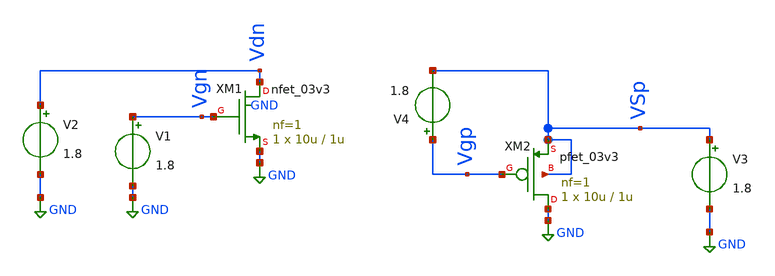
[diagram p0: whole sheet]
** sch_path: xschem/caracterizador/charac.sch
* Copyright 2022 GlobalFoundries PDK Authors
* Licensed under the Apache License, Version 2.0 (the "License");
* you may not use this file except in compliance with the License.
* You may obtain a copy of the License at
* https://www.apache.org/licenses/LICENSE-2.0
* Unless required by applicable law or agreed to in writing, software
* distributed under the License is distributed on an "AS IS" BASIS,
* WITHOUT WARRANTIES OR CONDITIONS OF ANY KIND, either express or implied.
* See the License for the specific language governing permissions and
* limitations under the License.
**.subckt charac
XM1 Vdn Vgn GND GND nfet_03v3 L=1u W=10u nf=1 ad='int((nf+1)/2) * W/nf * 0.18u' as='int((nf+2)/2) * W/nf * 0.18u'
+ pd='2*int((nf+1)/2) * (W/nf + 0.18u)' ps='2*int((nf+2)/2) * (W/nf + 0.18u)' nrd='0.18u / W' nrs='0.18u / W'
+ sa=0 sb=0 sd=0 m=1 par=1
XM2 GND Vgp VSp VSp pfet_03v3 L=1u W=10u nf=1 ad='int((nf+1)/2) * W/nf * 0.18u' as='int((nf+2)/2) * W/nf * 0.18u'
+ pd='2*int((nf+1)/2) * (W/nf + 0.18u)' ps='2*int((nf+2)/2) * (W/nf + 0.18u)' nrd='0.18u / W' nrs='0.18u / W'
+ sa=0 sb=0 sd=0 m=1 par=1
V1 Vgn GND 1.8
V2 Vdn GND 1.8
V3 VSp GND 1.8
V4 Vgp VSp 1.8
**** begin user architecture code


.include /home/ringosinye/eda/pdks/gf180mcuD/libs.tech/ngspice/design.ngspice
.lib /home/ringosinye/eda/pdks/gf180mcuD/libs.tech/ngspice/sm141064.ngspice typical
.param sw_stat_mismatch = 0




.control
save all

* Coloracion de graficas
set color0=white
set color1=black
set color2=blue
set color3=red
set xbrushwidth=2

* ========================================================
* PARAMETROS (lo unico que hay que editar)
* ========================================================
* gm/Id objetivo = nivel de inversion de cada transistor.
*   ~5-8   : inversion fuerte (rapido, poco gm por uA)
*   ~15    : inversion moderada
*   ~20-25 : inversion debil (maximo gm por uA, lento)
* Rango valido: ~3 a ~25 (el maximo fisico ronda 25-28).
set gmid_n_obj = 15
set gmid_p_obj = 15
* Este script no depende de W/L: el punto de trabajo se busca
* solo, igual que en Metricas_dc.

* ========================================================
* 1. NMOS: punto de polarizacion a gm/Id = gmid_n_obj
*    (VDS fijo = 1.65 V, barrido de VGS)
* ========================================================
alter V2 = 1.65
dc V1 0 3.3 0.01

let idn = abs(-i(V2)) + 1e-15
let gmn = deriv(idn)
let gmidn = gmn/idn

* cross=last toma el cruce en que gm/Id BAJA por el objetivo
meas dc id_n find idn when gmidn=$gmid_n_obj cross=last
meas dc vgs_n find v(vgn) when gmidn=$gmid_n_obj cross=last
set id_n_val = $&id_n
set vgs_n_val = $&vgs_n

* ========================================================
* 2. NMOS: analisis AC en ese punto (fT, gm y Cgg)
* ========================================================
alter V1 = $vgs_n_val
alter V1 acmag = 1
ac dec 20 1k 100G

* Ganancia de corriente en cortocircuito H21 = i(drenaje) / i(compuerta)
let h21_n = abs(i(V2) / i(V1))
* Cgg = Im(i compuerta) / w, con 1 V de AC en la compuerta
let cgg_n = abs(imag(i(V1))) / (2*pi*frequency)
* gm = |i(drenaje)| con 1 V de AC en la compuerta
let gm_ac_n = abs(i(V2))

* fT = frecuencia en que H21 cae a 1 (0 dB)
meas ac fT_n when h21_n=1
set fT_n_val = $&fT_n

* Cgg a 100 kHz (bien por debajo de fT) y gm a 1 kHz
meas ac cgg_n_m find cgg_n at=1e5
meas ac gm_n_m find gm_ac_n at=1e3

set cgg_n_val = $&cgg_n_m
set gm_n_val = $&gm_n_m

* Evita AC cruzado en la seccion PMOS
alter V1 acmag = 0

* ========================================================
* 3. PMOS: punto de polarizacion a gm/Id = gmid_p_obj
*    (VSD fijo = 1.65 V, barrido de VSG)
* ========================================================
alter V3 = 1.65
dc V4 0 -3.3 -0.01

let idp = abs(i(V3)) + 1e-15
let gmp = abs(deriv(idp))
let gmidp = gmp/idp
let vgsp = vgp-vsp

meas dc id_p find idp when gmidp=$gmid_p_obj cross=last
meas dc vgs_p find vgsp when gmidp=$gmid_p_obj cross=last
set id_p_val = $&id_p
set vgs_p_val = $&vgs_p

* ========================================================
* 4. PMOS: analisis AC en ese punto (fT, gm y Cgg)
* ========================================================
alter V4 = $vgs_p_val
alter V4 acmag = 1
ac dec 20 1k 100G

let h21_p = abs(i(V3) / i(V4))
let cgg_p = abs(imag(i(V4))) / (2*pi*frequency)
let gm_ac_p = abs(i(V3))

meas ac fT_p when h21_p=1
set fT_p_val = $&fT_p

meas ac cgg_p_m find cgg_p at=1e5
meas ac gm_p_m find gm_ac_p at=1e3

set cgg_p_val = $&cgg_p_m
set gm_p_val = $&gm_p_m

* Comprobaciones de consistencia
let gmid_chk_n = $gm_n_val / $id_n_val
let gmid_chk_p = $gm_p_val / $id_p_val
let ft_chk_n = $gm_n_val / (2*pi*$cgg_n_val)
let ft_chk_p = $gm_p_val / (2*pi*$cgg_p_val)

* Graficar ganancia de corriente en dB vs frecuencia
plot db(ac1.h21_n) db(ac2.h21_p) xlog title 'Ganancia de Corriente H21 (fT)' xlabel 'Frecuencia (Hz)'
+ ylabel 'H21 (dB)'

* --- IMPRIMIR RESULTADOS EN CONSOLA ---
echo ================ RESULTADOS AC ================
echo ---- NMOS (gm/Id objetivo = $gmid_n_obj) ----
echo Id = $id_n_val A
echo Vgs = $vgs_n_val V
echo fT = $fT_n_val Hz
echo gm = $gm_n_val S
echo Cgg = $cgg_n_val F
echo Chequeo gm/Id (debe dar el objetivo) = $&gmid_chk_n
echo Chequeo fT = gm/(2pi Cgg) = $&ft_chk_n Hz
echo ---- PMOS (gm/Id objetivo = $gmid_p_obj) ----
echo Id = $id_p_val A
echo Vgs = $vgs_p_val V
echo fT = $fT_p_val Hz
echo gm = $gm_p_val S
echo Cgg = $cgg_p_val F
echo Chequeo gm/Id (debe dar el objetivo) = $&gmid_chk_p
echo Chequeo fT = gm/(2pi Cgg) = $&ft_chk_p Hz
echo ===============================================
.endc


**** end user architecture code
**.ends
.GLOBAL GND
.end
